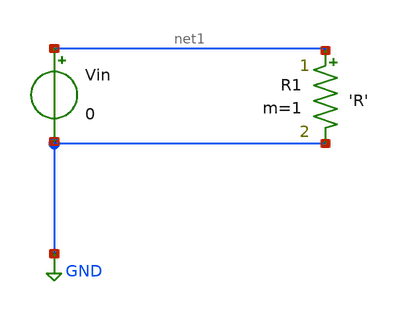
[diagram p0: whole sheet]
** sch_path: test-optimization.sch
**.subckt test-optimization
Vin net1 GND 0
R1 net1 GND 'R' m=1
**** begin user architecture code


.csparam R=10

.options savecurrents
.control
save all


let step=1
let maxval=20
let currval=10

let min_diff=100
let bestval=currval

while currval < maxval
	alterparam R=10
	reset
	dc vin 0 1.8 1m

	let currval=currval + step


end

print min_diff
print best_w




.endc


**** end user architecture code
**.ends
.GLOBAL GND
.end
